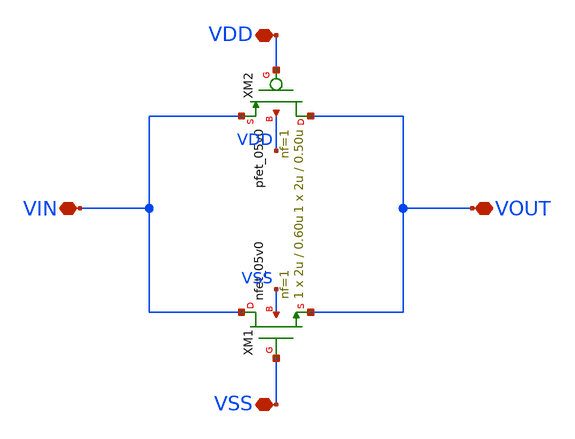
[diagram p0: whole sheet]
** sch_path: designs/libs/core_test/test_tg/test_tg.sch
**.subckt test_tg VIN VOUT VDD VSS
*.iopin VIN
*.iopin VOUT
*.iopin VDD
*.iopin VSS
XM1 VIN VSS VOUT VSS nfet_05v0 L=0.60u W=2u nf=1 ad='int((nf+1)/2) * W/nf * 0.18u' as='int((nf+2)/2) * W/nf * 0.18u'
+ pd='2*int((nf+1)/2) * (W/nf + 0.18u)' ps='2*int((nf+2)/2) * (W/nf + 0.18u)' nrd='0.18u / W' nrs='0.18u / W'
+ sa=0 sb=0 sd=0 m=1
XM2 VOUT VDD VIN VDD pfet_05v0 L=0.50u W=2u nf=1 ad='int((nf+1)/2) * W/nf * 0.18u' as='int((nf+2)/2) * W/nf * 0.18u'
+ pd='2*int((nf+1)/2) * (W/nf + 0.18u)' ps='2*int((nf+2)/2) * (W/nf + 0.18u)' nrd='0.18u / W' nrs='0.18u / W'
+ sa=0 sb=0 sd=0 m=1
**.ends
.end
